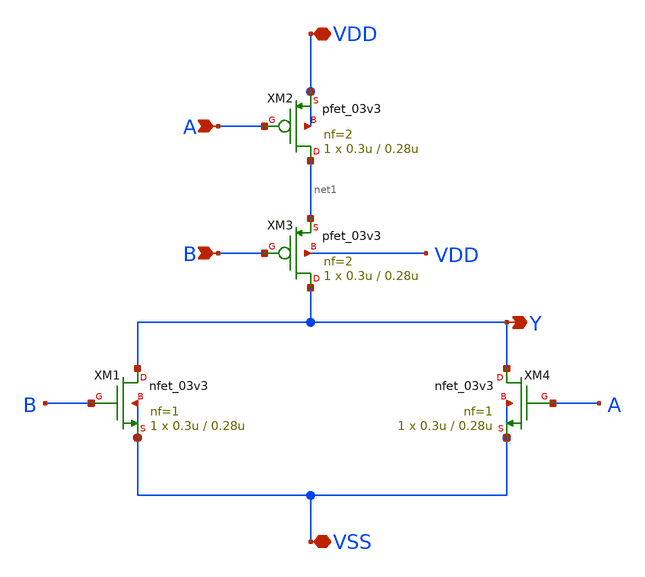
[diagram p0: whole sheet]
** sch_path: designs/libs/core_test/test_nor/test_nor.sch
**.subckt test_nor VDD VSS Y A B
*.iopin VDD
*.iopin VSS
*.opin Y
*.ipin A
*.ipin B
XM1 Y B VSS VSS nfet_03v3 L=0.28u W=0.3u nf=1 ad='int((nf+1)/2) * W/nf * 0.18u' as='int((nf+2)/2) * W/nf * 0.18u'
+ pd='2*int((nf+1)/2) * (W/nf + 0.18u)' ps='2*int((nf+2)/2) * (W/nf + 0.18u)' nrd='0.18u / W' nrs='0.18u / W'
+ sa=0 sb=0 sd=0 m=1
XM2 net1 A VDD VDD pfet_03v3 L=0.28u W=0.3u nf=2 ad='int((nf+1)/2) * W/nf * 0.18u' as='int((nf+2)/2) * W/nf * 0.18u'
+ pd='2*int((nf+1)/2) * (W/nf + 0.18u)' ps='2*int((nf+2)/2) * (W/nf + 0.18u)' nrd='0.18u / W' nrs='0.18u / W'
+ sa=0 sb=0 sd=0 m=1
XM3 Y B net1 VDD pfet_03v3 L=0.28u W=0.3u nf=2 ad='int((nf+1)/2) * W/nf * 0.18u' as='int((nf+2)/2) * W/nf * 0.18u'
+ pd='2*int((nf+1)/2) * (W/nf + 0.18u)' ps='2*int((nf+2)/2) * (W/nf + 0.18u)' nrd='0.18u / W' nrs='0.18u / W'
+ sa=0 sb=0 sd=0 m=1
XM4 Y A VSS VSS nfet_03v3 L=0.28u W=0.3u nf=1 ad='int((nf+1)/2) * W/nf * 0.18u' as='int((nf+2)/2) * W/nf * 0.18u'
+ pd='2*int((nf+1)/2) * (W/nf + 0.18u)' ps='2*int((nf+2)/2) * (W/nf + 0.18u)' nrd='0.18u / W' nrs='0.18u / W'
+ sa=0 sb=0 sd=0 m=1
**.ends
.end
